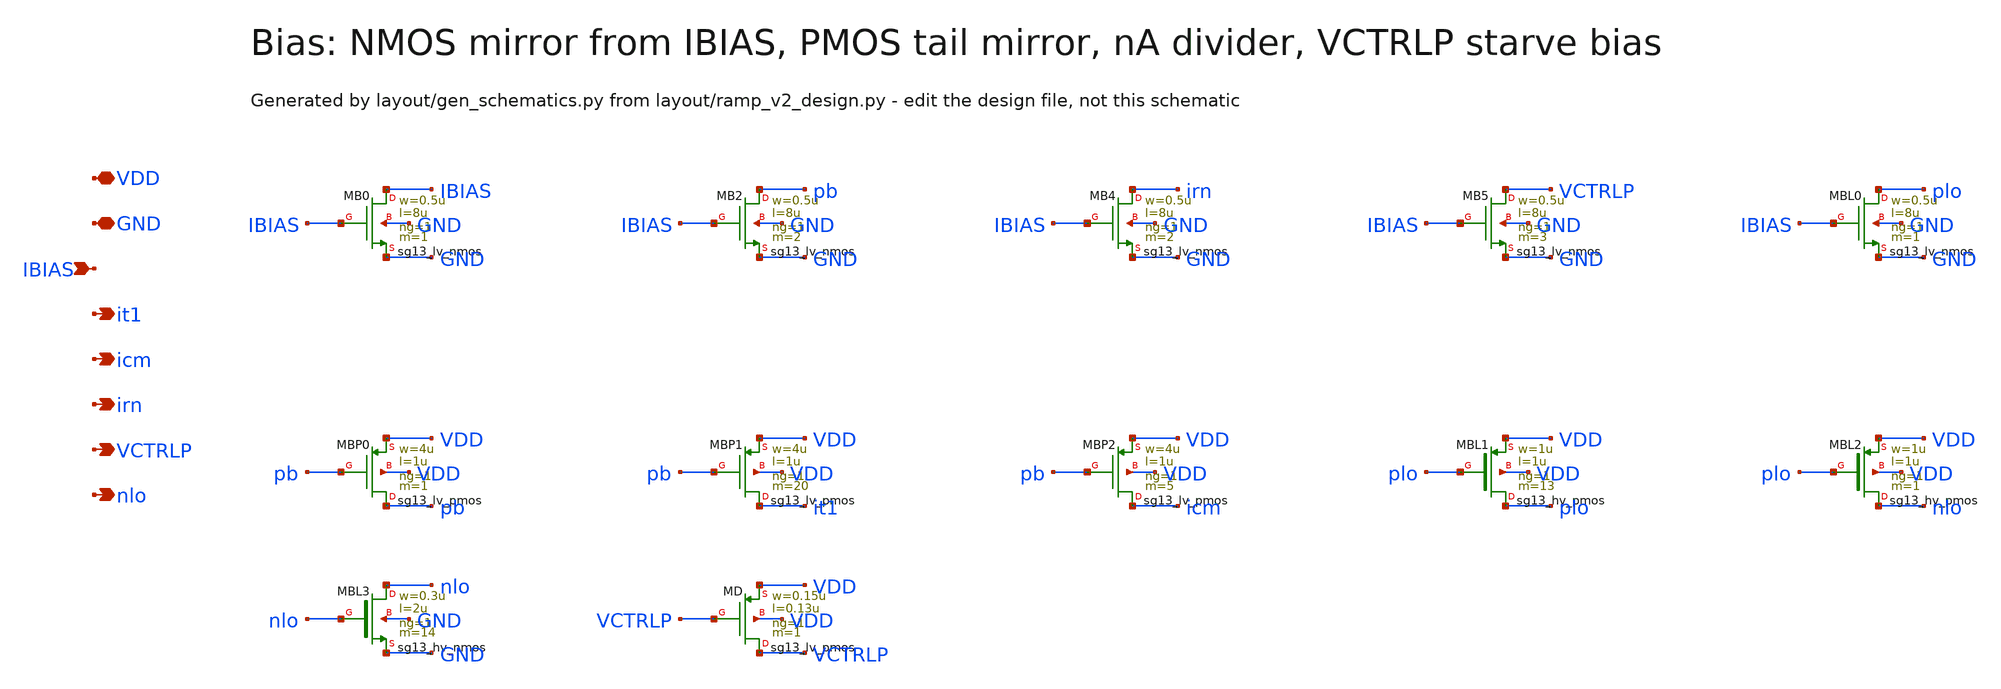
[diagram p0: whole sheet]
** sch_path: Design Files/RAMP/RAMP-V2/BIAS_V2.sch
**.subckt BIAS_V2 VDD GND IBIAS it1 icm irn VCTRLP nlo
*.iopin VDD
*.iopin GND
*.ipin IBIAS
*.opin it1
*.opin icm
*.opin irn
*.opin VCTRLP
*.opin nlo
XMB0 IBIAS IBIAS GND GND sg13_lv_nmos w=0.5u l=8u ng=1 m=1 mm_ok=1
XMB2 pb IBIAS GND GND sg13_lv_nmos w=0.5u l=8u ng=1 m=2 mm_ok=1
XMB4 irn IBIAS GND GND sg13_lv_nmos w=0.5u l=8u ng=1 m=2 mm_ok=1
XMB5 VCTRLP IBIAS GND GND sg13_lv_nmos w=0.5u l=8u ng=1 m=3 mm_ok=1
XMBL0 plo IBIAS GND GND sg13_lv_nmos w=0.5u l=8u ng=1 m=1 mm_ok=1
XMBP0 pb pb VDD VDD sg13_lv_pmos w=4u l=1u ng=1 m=1 mm_ok=1
XMBP1 it1 pb VDD VDD sg13_lv_pmos w=4u l=1u ng=1 m=20 mm_ok=1
XMBP2 icm pb VDD VDD sg13_lv_pmos w=4u l=1u ng=1 m=5 mm_ok=1
XMBL1 plo plo VDD VDD sg13_hv_pmos w=1u l=1u ng=1 m=13 mm_ok=1
XMBL2 nlo plo VDD VDD sg13_hv_pmos w=1u l=1u ng=1 m=1 mm_ok=1
XMBL3 nlo nlo GND GND sg13_hv_nmos w=0.3u l=2u ng=1 m=14 mm_ok=1
XMD VCTRLP VCTRLP VDD VDD sg13_lv_pmos w=0.15u l=0.13u ng=1 m=1 mm_ok=1
**.ends
.end
